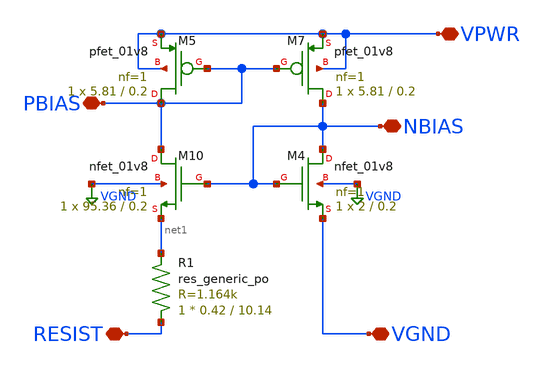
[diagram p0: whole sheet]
** sch_path: project2/bootstrap/sky130_hilas_Bootstrap01.sch
**.subckt sky130_hilas_Bootstrap01 VPWR NBIAS PBIAS VGND RESIST
*.iopin VPWR
*.iopin NBIAS
*.iopin PBIAS
*.iopin VGND
*.iopin RESIST
XM4 NBIAS NBIAS VGND VGND sky130_fd_pr__nfet_01v8 L=0.2 W=2 nf=1 ad='int((nf+1)/2) * W/nf * 0.29' as='int((nf+2)/2) * W/nf * 0.29'
+ pd='2*int((nf+1)/2) * (W/nf + 0.29)' ps='2*int((nf+2)/2) * (W/nf + 0.29)' nrd='0.29 / W' nrs='0.29 / W'
+ sa=0 sb=0 sd=0 mult=1 m=1
XM7 NBIAS PBIAS VPWR VPWR sky130_fd_pr__pfet_01v8 L=0.2 W=5.81 nf=1 ad='int((nf+1)/2) * W/nf * 0.29'
+ as='int((nf+2)/2) * W/nf * 0.29' pd='2*int((nf+1)/2) * (W/nf + 0.29)' ps='2*int((nf+2)/2) * (W/nf + 0.29)'
+ nrd='0.29 / W' nrs='0.29 / W' sa=0 sb=0 sd=0 mult=1 m=1
XM10 PBIAS NBIAS net1 VGND sky130_fd_pr__nfet_01v8 L=0.2 W=95.36 nf=1 ad='int((nf+1)/2) * W/nf * 0.29'
+ as='int((nf+2)/2) * W/nf * 0.29' pd='2*int((nf+1)/2) * (W/nf + 0.29)' ps='2*int((nf+2)/2) * (W/nf + 0.29)'
+ nrd='0.29 / W' nrs='0.29 / W' sa=0 sb=0 sd=0 mult=1 m=1
XM5 PBIAS PBIAS VPWR VPWR sky130_fd_pr__pfet_01v8 L=0.2 W=5.81 nf=1 ad='int((nf+1)/2) * W/nf * 0.29'
+ as='int((nf+2)/2) * W/nf * 0.29' pd='2*int((nf+1)/2) * (W/nf + 0.29)' ps='2*int((nf+2)/2) * (W/nf + 0.29)'
+ nrd='0.29 / W' nrs='0.29 / W' sa=0 sb=0 sd=0 mult=1 m=1
XR1 RESIST net1 sky130_fd_pr__res_generic_po W=0.42 L=10.14 m=1
**.ends
.GLOBAL VGND
.end
